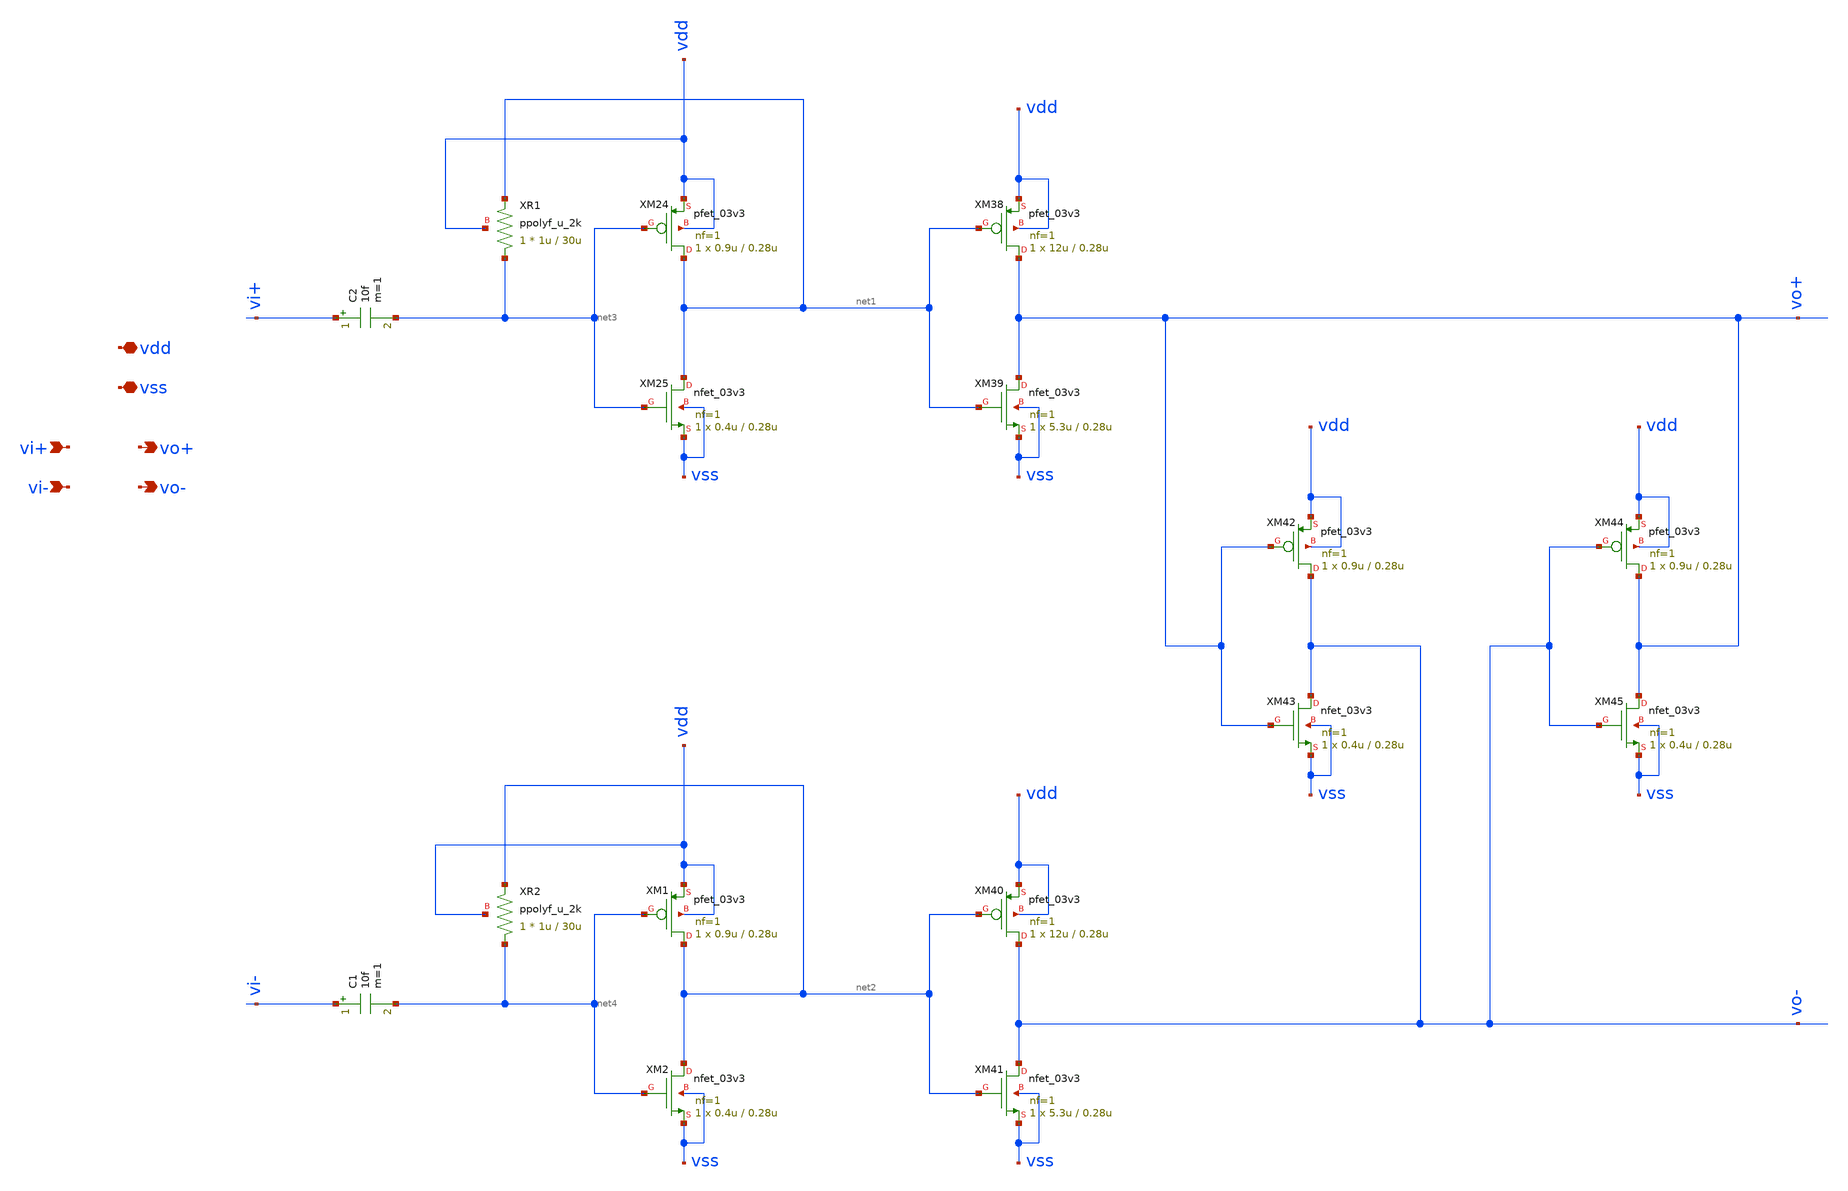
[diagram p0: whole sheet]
** sch_path: xschem/opbuffer.sch
**.subckt opbuffer vdd vss vi+ vi- vo+ vo-
*.iopin vdd
*.iopin vss
*.ipin vi+
*.ipin vi-
*.opin vo+
*.opin vo-
XM38 vo+ net1 vdd vdd pfet_03v3 L=0.28u W=12u nf=1 ad='int((nf+1)/2) * W/nf * 0.18u' as='int((nf+2)/2) * W/nf * 0.18u'
+ pd='2*int((nf+1)/2) * (W/nf + 0.18u)' ps='2*int((nf+2)/2) * (W/nf + 0.18u)' nrd='0.18u / W' nrs='0.18u / W'
+ sa=0 sb=0 sd=0 m=1
XM39 vo+ net1 vss vss nfet_03v3 L=0.28u W=5.3u nf=1 ad='int((nf+1)/2) * W/nf * 0.18u' as='int((nf+2)/2) * W/nf * 0.18u'
+ pd='2*int((nf+1)/2) * (W/nf + 0.18u)' ps='2*int((nf+2)/2) * (W/nf + 0.18u)' nrd='0.18u / W' nrs='0.18u / W'
+ sa=0 sb=0 sd=0 m=1
XM40 vo- net2 vdd vdd pfet_03v3 L=0.28u W=12u nf=1 ad='int((nf+1)/2) * W/nf * 0.18u' as='int((nf+2)/2) * W/nf * 0.18u'
+ pd='2*int((nf+1)/2) * (W/nf + 0.18u)' ps='2*int((nf+2)/2) * (W/nf + 0.18u)' nrd='0.18u / W' nrs='0.18u / W'
+ sa=0 sb=0 sd=0 m=1
XM41 vo- net2 vss vss nfet_03v3 L=0.28u W=5.3u nf=1 ad='int((nf+1)/2) * W/nf * 0.18u' as='int((nf+2)/2) * W/nf * 0.18u'
+ pd='2*int((nf+1)/2) * (W/nf + 0.18u)' ps='2*int((nf+2)/2) * (W/nf + 0.18u)' nrd='0.18u / W' nrs='0.18u / W'
+ sa=0 sb=0 sd=0 m=1
XM42 vo- vo+ vdd vdd pfet_03v3 L=0.28u W=0.9u nf=1 ad='int((nf+1)/2) * W/nf * 0.18u' as='int((nf+2)/2) * W/nf * 0.18u'
+ pd='2*int((nf+1)/2) * (W/nf + 0.18u)' ps='2*int((nf+2)/2) * (W/nf + 0.18u)' nrd='0.18u / W' nrs='0.18u / W'
+ sa=0 sb=0 sd=0 m=1
XM43 vo- vo+ vss vss nfet_03v3 L=0.28u W=0.4u nf=1 ad='int((nf+1)/2) * W/nf * 0.18u' as='int((nf+2)/2) * W/nf * 0.18u'
+ pd='2*int((nf+1)/2) * (W/nf + 0.18u)' ps='2*int((nf+2)/2) * (W/nf + 0.18u)' nrd='0.18u / W' nrs='0.18u / W'
+ sa=0 sb=0 sd=0 m=1
XM44 vo+ vo- vdd vdd pfet_03v3 L=0.28u W=0.9u nf=1 ad='int((nf+1)/2) * W/nf * 0.18u' as='int((nf+2)/2) * W/nf * 0.18u'
+ pd='2*int((nf+1)/2) * (W/nf + 0.18u)' ps='2*int((nf+2)/2) * (W/nf + 0.18u)' nrd='0.18u / W' nrs='0.18u / W'
+ sa=0 sb=0 sd=0 m=1
XM45 vo+ vo- vss vss nfet_03v3 L=0.28u W=0.4u nf=1 ad='int((nf+1)/2) * W/nf * 0.18u' as='int((nf+2)/2) * W/nf * 0.18u'
+ pd='2*int((nf+1)/2) * (W/nf + 0.18u)' ps='2*int((nf+2)/2) * (W/nf + 0.18u)' nrd='0.18u / W' nrs='0.18u / W'
+ sa=0 sb=0 sd=0 m=1
XM24 net1 net3 vdd vdd pfet_03v3 L=0.28u W=0.9u nf=1 ad='int((nf+1)/2) * W/nf * 0.18u' as='int((nf+2)/2) * W/nf * 0.18u'
+ pd='2*int((nf+1)/2) * (W/nf + 0.18u)' ps='2*int((nf+2)/2) * (W/nf + 0.18u)' nrd='0.18u / W' nrs='0.18u / W'
+ sa=0 sb=0 sd=0 m=1
XM25 net1 net3 vss vss nfet_03v3 L=0.28u W=0.4u nf=1 ad='int((nf+1)/2) * W/nf * 0.18u' as='int((nf+2)/2) * W/nf * 0.18u'
+ pd='2*int((nf+1)/2) * (W/nf + 0.18u)' ps='2*int((nf+2)/2) * (W/nf + 0.18u)' nrd='0.18u / W' nrs='0.18u / W'
+ sa=0 sb=0 sd=0 m=1
C2 vi+ net3 10f m=1
XM1 net2 net4 vdd vdd pfet_03v3 L=0.28u W=0.9u nf=1 ad='int((nf+1)/2) * W/nf * 0.18u' as='int((nf+2)/2) * W/nf * 0.18u'
+ pd='2*int((nf+1)/2) * (W/nf + 0.18u)' ps='2*int((nf+2)/2) * (W/nf + 0.18u)' nrd='0.18u / W' nrs='0.18u / W'
+ sa=0 sb=0 sd=0 m=1
XM2 net2 net4 vss vss nfet_03v3 L=0.28u W=0.4u nf=1 ad='int((nf+1)/2) * W/nf * 0.18u' as='int((nf+2)/2) * W/nf * 0.18u'
+ pd='2*int((nf+1)/2) * (W/nf + 0.18u)' ps='2*int((nf+2)/2) * (W/nf + 0.18u)' nrd='0.18u / W' nrs='0.18u / W'
+ sa=0 sb=0 sd=0 m=1
C1 vi- net4 10f m=1
XR1 net3 net1 vdd ppolyf_u_2k r_width=1u r_length=30u m=1
XR2 net4 net2 vdd ppolyf_u_2k r_width=1u r_length=30u m=1
**.ends
.end
